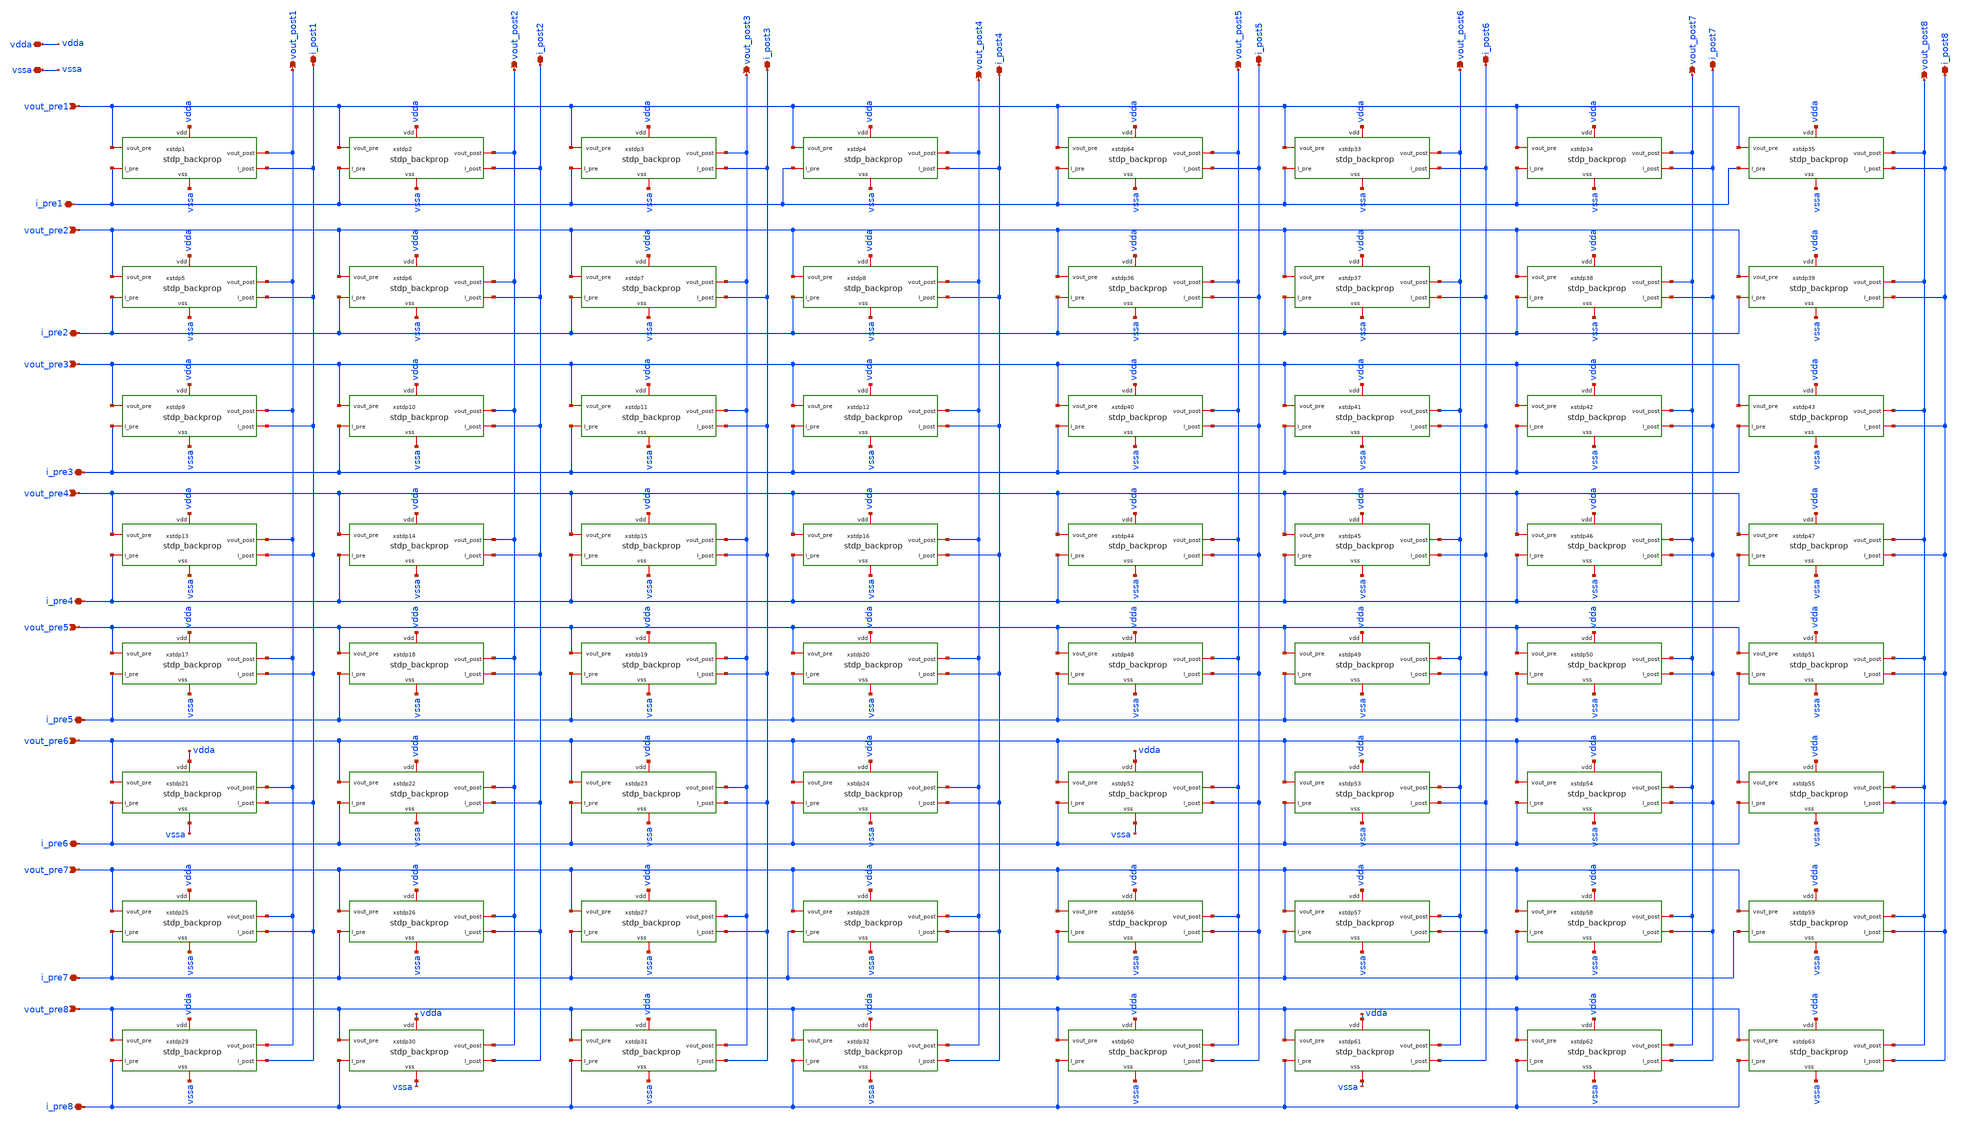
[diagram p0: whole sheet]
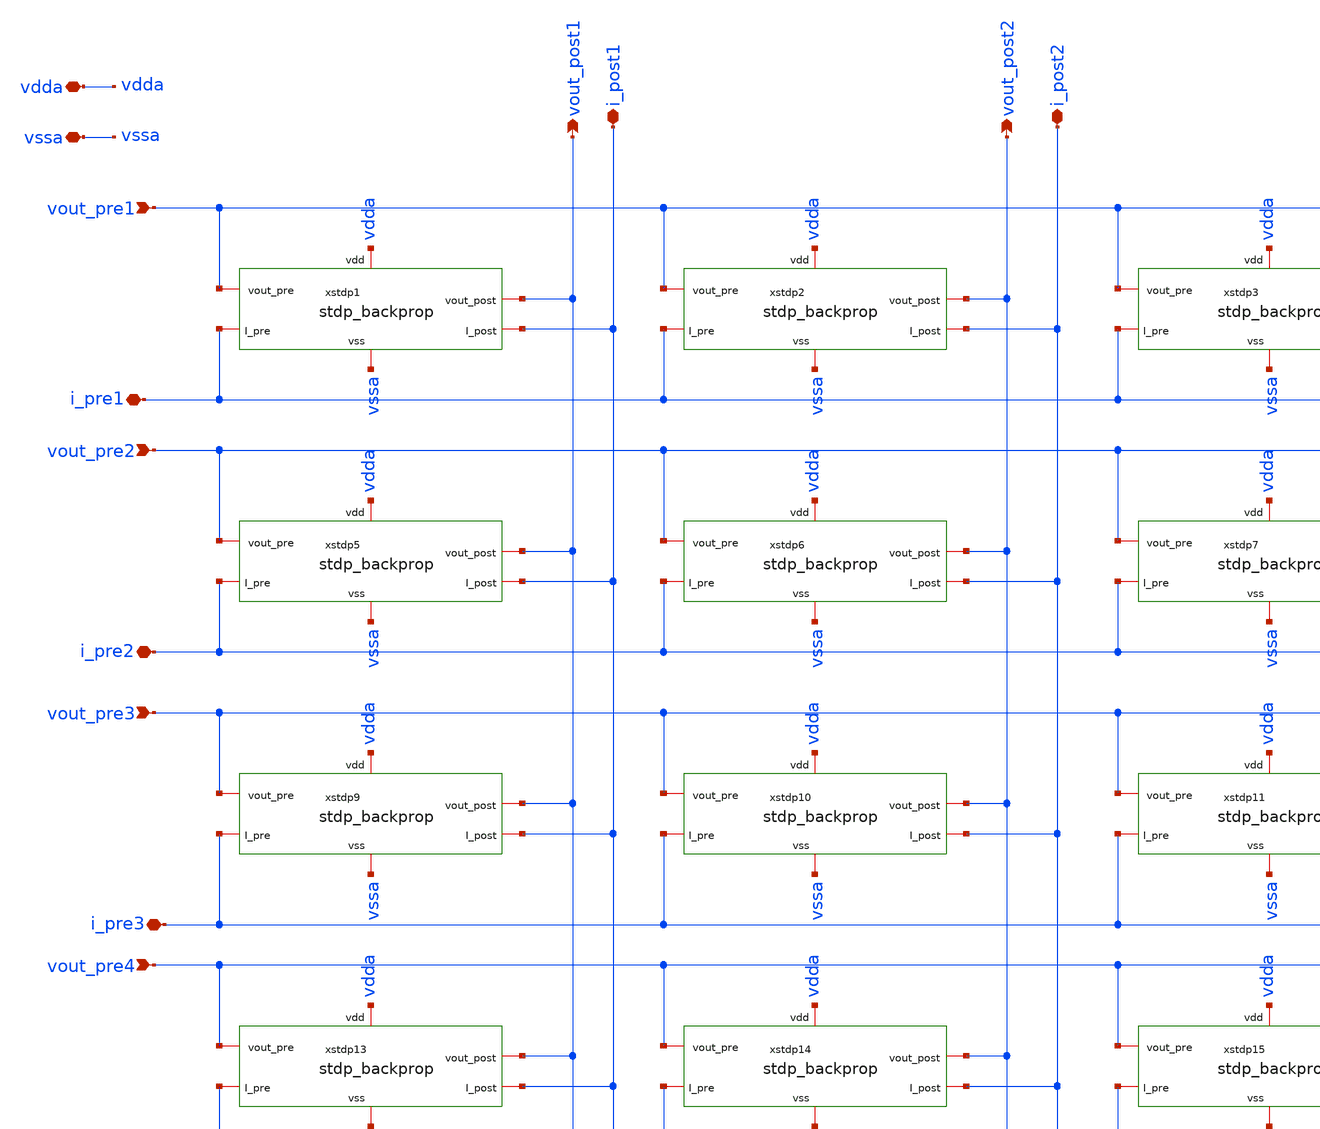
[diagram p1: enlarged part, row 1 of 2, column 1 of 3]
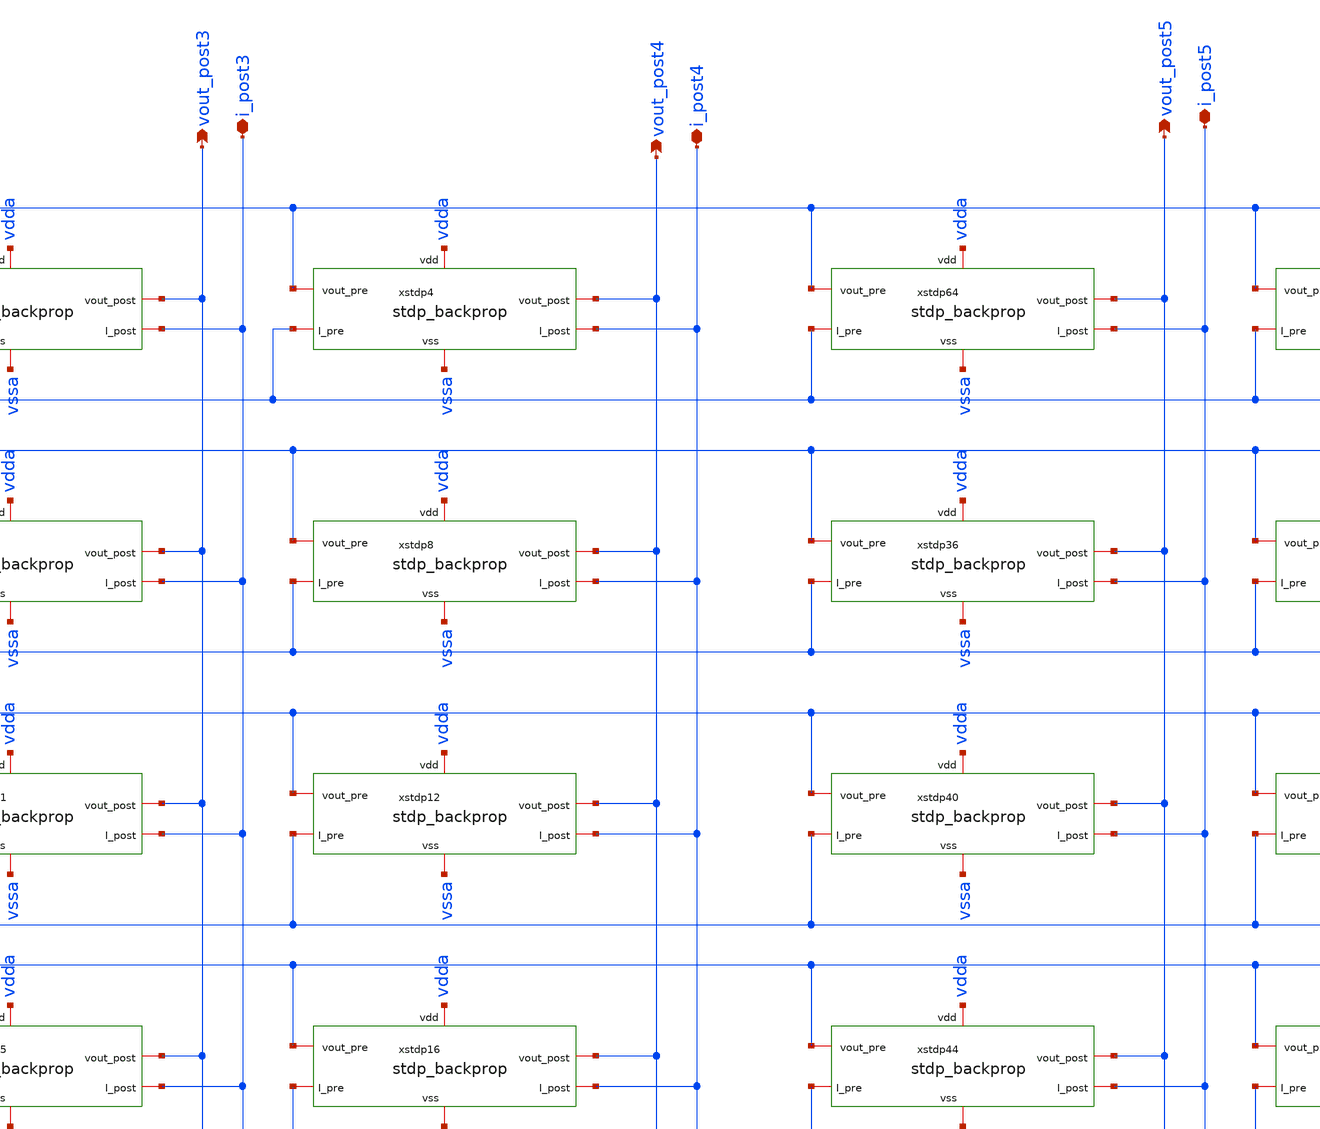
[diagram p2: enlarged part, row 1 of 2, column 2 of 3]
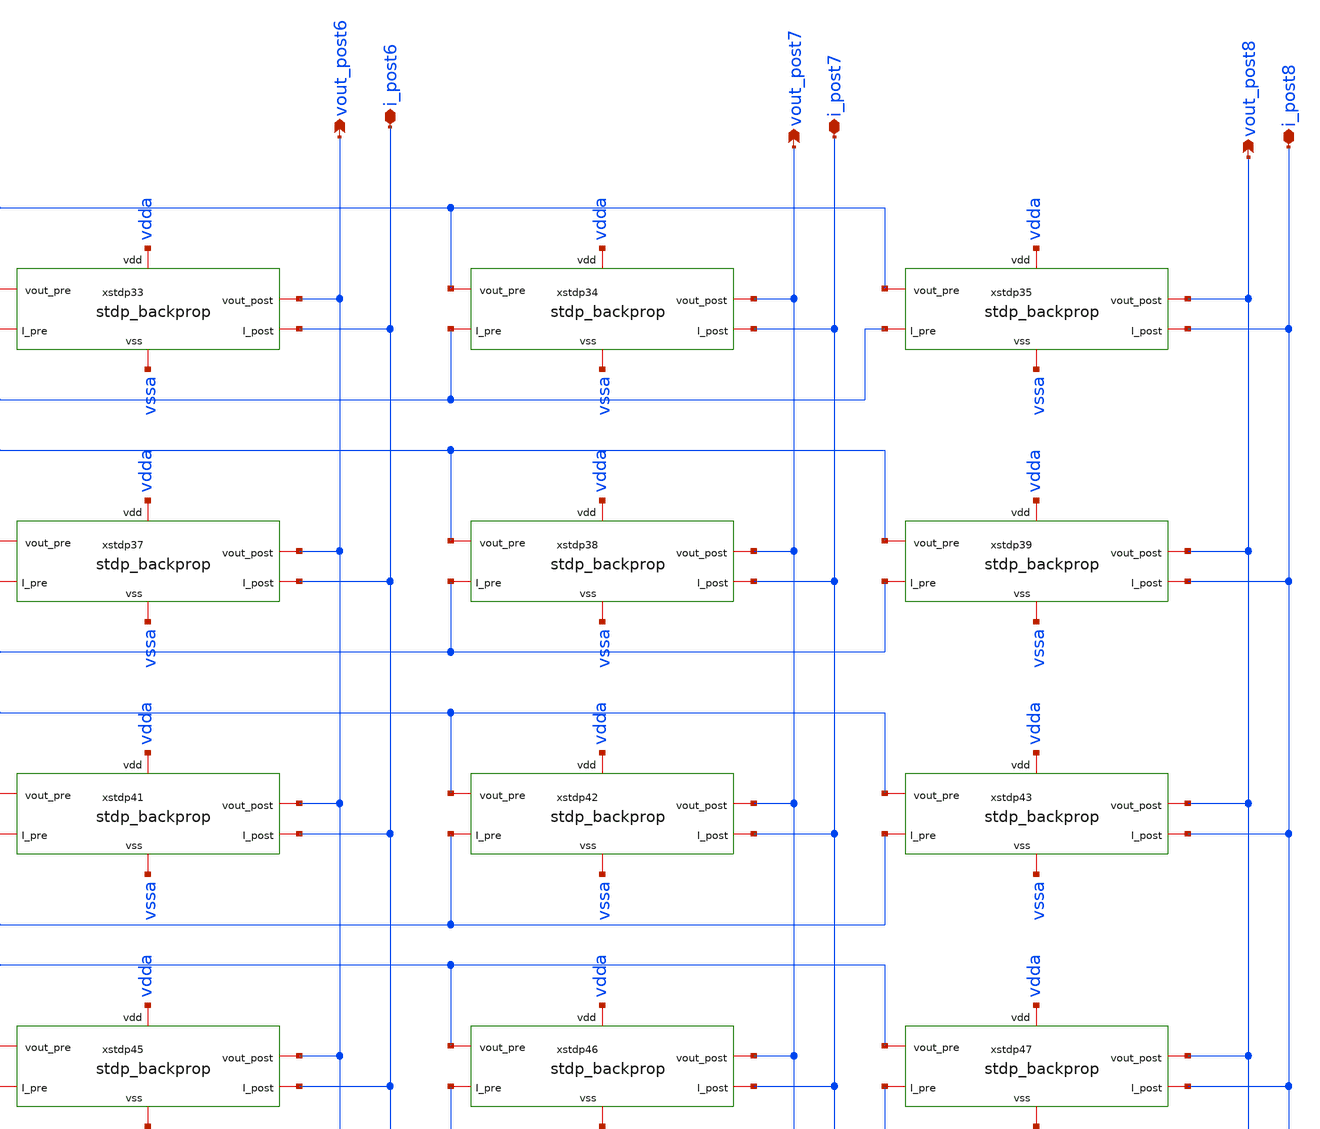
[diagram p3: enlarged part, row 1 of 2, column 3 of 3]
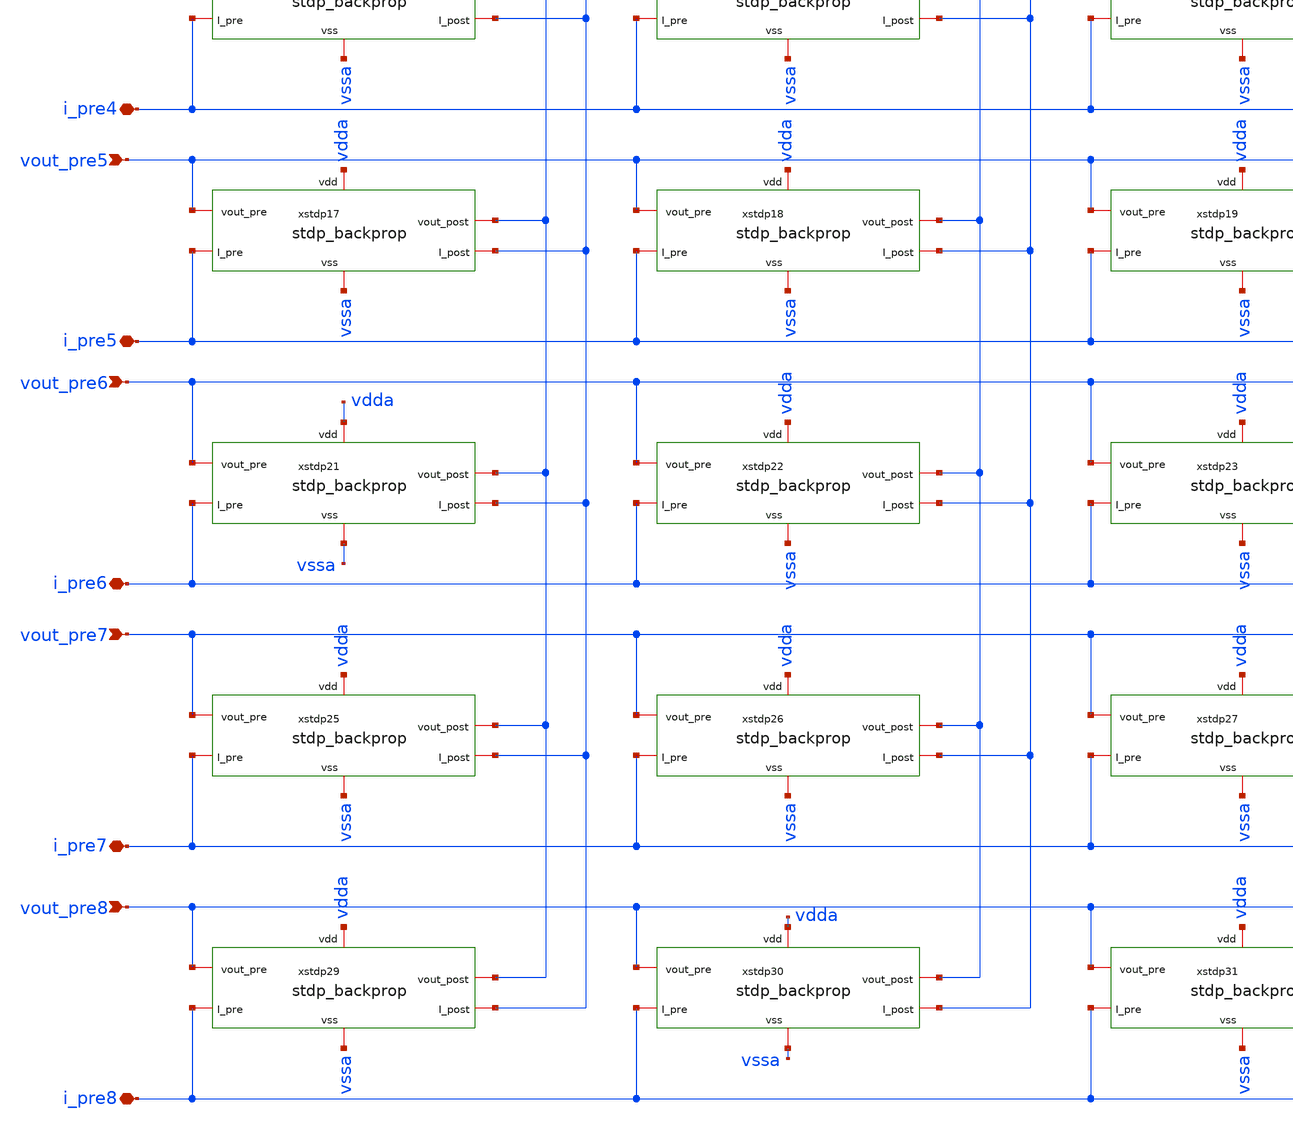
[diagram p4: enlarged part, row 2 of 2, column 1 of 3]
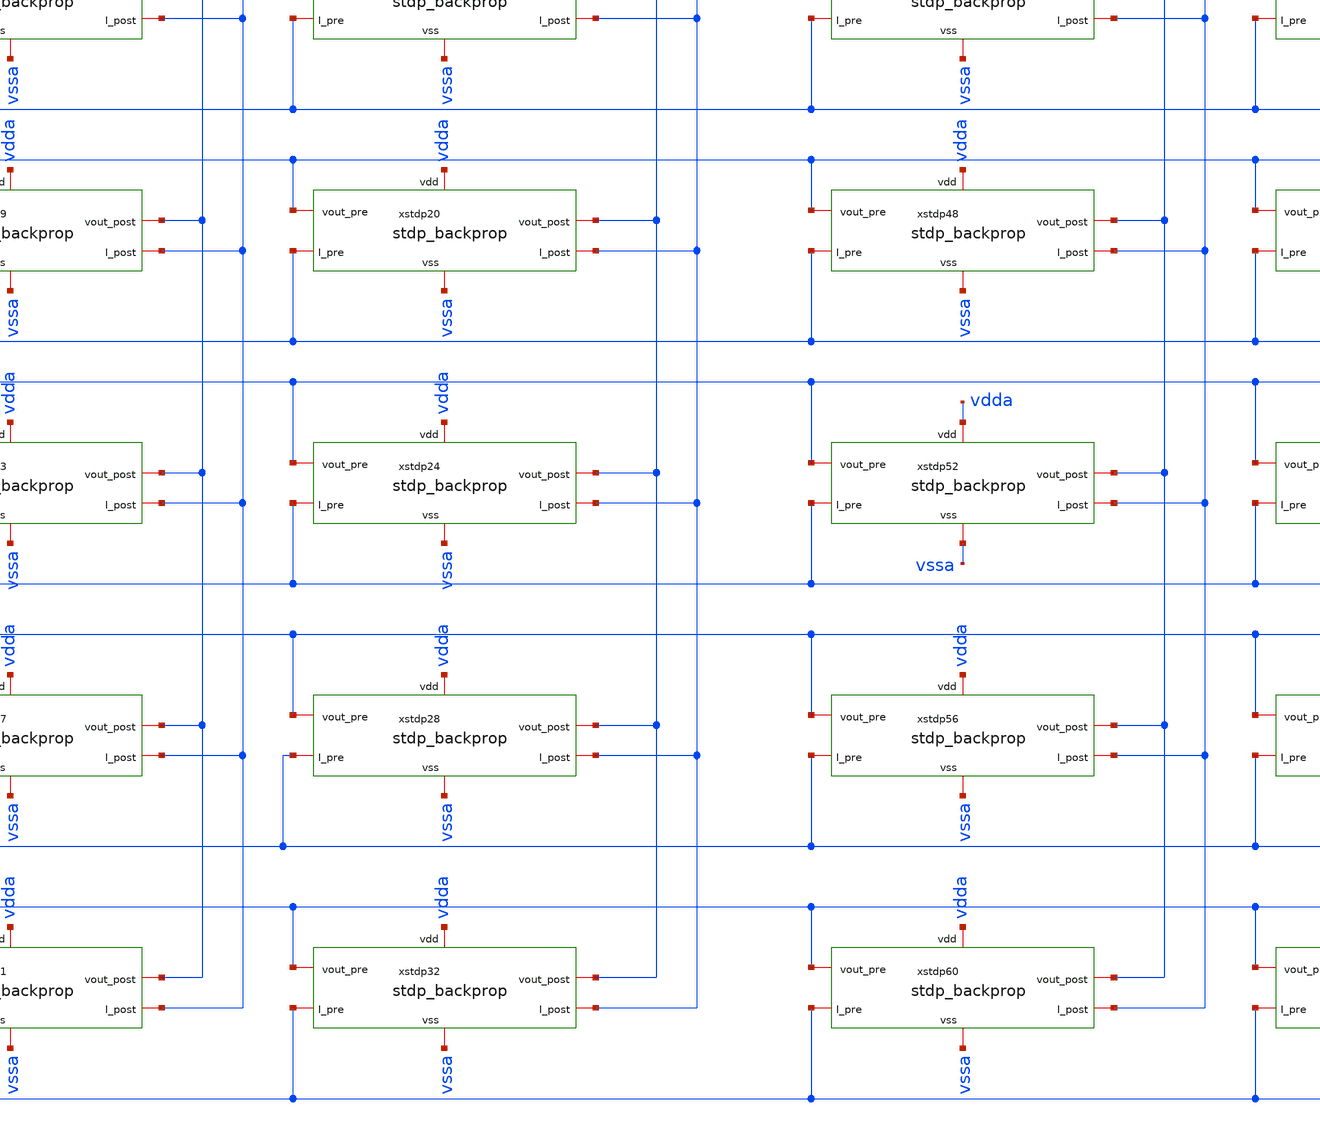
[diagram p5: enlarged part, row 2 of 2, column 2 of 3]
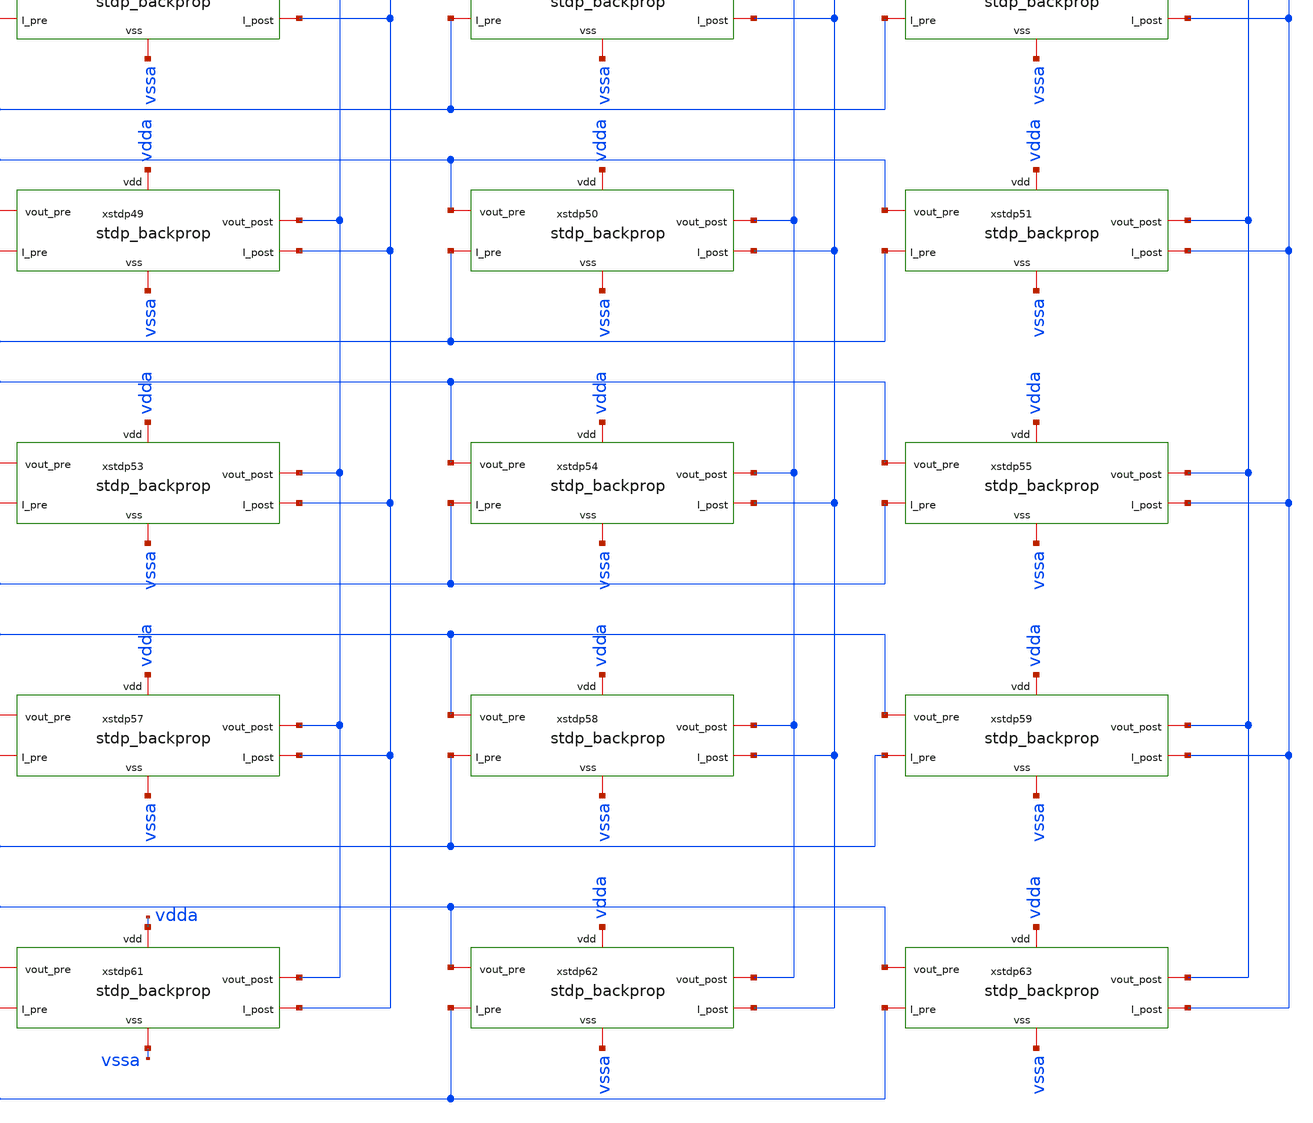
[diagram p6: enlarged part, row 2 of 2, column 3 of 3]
** sch_path: Synapse/stdp_backprop_8x8.sch
**.subckt stdp_backprop_8x8 vout_pre1 vout_post1 vdda vssa i_post1 i_post3 i_post4 vout_pre2
*+ vout_pre3 vout_pre4 vout_post2 vout_post3 vout_post4 i_post2 vout_pre5 vout_pre6 vout_pre7 vout_pre8 i_pre1
*+ i_pre2 i_pre3 i_pre4 i_pre5 i_pre6 i_pre7 i_pre8 vout_post5 i_post5 i_post7 i_post8 vout_post6 vout_post7
*+ vout_post8 i_post6
*.ipin vout_pre1
*.opin vout_post1
*.iopin vdda
*.iopin vssa
*.iopin i_post1
*.iopin i_post3
*.iopin i_post4
*.ipin vout_pre2
*.ipin vout_pre3
*.ipin vout_pre4
*.opin vout_post2
*.opin vout_post3
*.opin vout_post4
*.iopin i_post2
*.ipin vout_pre5
*.ipin vout_pre6
*.ipin vout_pre7
*.ipin vout_pre8
*.iopin i_pre1
*.iopin i_pre2
*.iopin i_pre3
*.iopin i_pre4
*.iopin i_pre5
*.iopin i_pre6
*.iopin i_pre7
*.iopin i_pre8
*.opin vout_post5
*.iopin i_post5
*.iopin i_post7
*.iopin i_post8
*.opin vout_post6
*.opin vout_post7
*.opin vout_post8
*.iopin i_post6
xstdp2 vdda vssa vout_pre1 vout_post2 i_post2 i_pre1 stdp_backprop
xstdp3 vdda vssa vout_pre1 vout_post3 i_post3 i_pre1 stdp_backprop
xstdp4 vdda vssa vout_pre1 vout_post4 i_post4 i_pre1 stdp_backprop
xstdp5 vdda vssa vout_pre2 vout_post1 i_post1 i_pre2 stdp_backprop
xstdp6 vdda vssa vout_pre2 vout_post2 i_post2 i_pre2 stdp_backprop
xstdp7 vdda vssa vout_pre2 vout_post3 i_post3 i_pre2 stdp_backprop
xstdp8 vdda vssa vout_pre2 vout_post4 i_post4 i_pre2 stdp_backprop
xstdp9 vdda vssa vout_pre3 vout_post1 i_post1 i_pre3 stdp_backprop
xstdp10 vdda vssa vout_pre3 vout_post2 i_post2 i_pre3 stdp_backprop
xstdp11 vdda vssa vout_pre3 vout_post3 i_post3 i_pre3 stdp_backprop
xstdp12 vdda vssa vout_pre3 vout_post4 i_post4 i_pre3 stdp_backprop
xstdp13 vdda vssa vout_pre4 vout_post1 i_post1 i_pre4 stdp_backprop
xstdp14 vdda vssa vout_pre4 vout_post2 i_post2 i_pre4 stdp_backprop
xstdp15 vdda vssa vout_pre4 vout_post3 i_post3 i_pre4 stdp_backprop
xstdp16 vdda vssa vout_pre4 vout_post4 i_post4 i_pre4 stdp_backprop
xstdp17 vdda vssa vout_pre5 vout_post1 i_post1 i_pre5 stdp_backprop
xstdp18 vdda vssa vout_pre5 vout_post2 i_post2 i_pre5 stdp_backprop
xstdp19 vdda vssa vout_pre5 vout_post3 i_post3 i_pre5 stdp_backprop
xstdp20 vdda vssa vout_pre5 vout_post4 i_post4 i_pre5 stdp_backprop
xstdp21 vdda vssa vout_pre6 vout_post1 i_post1 i_pre6 stdp_backprop
xstdp22 vdda vssa vout_pre6 vout_post2 i_post2 i_pre6 stdp_backprop
xstdp23 vdda vssa vout_pre6 vout_post3 i_post3 i_pre6 stdp_backprop
xstdp24 vdda vssa vout_pre6 vout_post4 i_post4 i_pre6 stdp_backprop
xstdp25 vdda vssa vout_pre7 vout_post1 i_post1 i_pre7 stdp_backprop
xstdp26 vdda vssa vout_pre7 vout_post2 i_post2 i_pre7 stdp_backprop
xstdp27 vdda vssa vout_pre7 vout_post3 i_post3 i_pre7 stdp_backprop
xstdp28 vdda vssa vout_pre7 vout_post4 i_post4 i_pre7 stdp_backprop
xstdp29 vdda vssa vout_pre8 vout_post1 i_post1 i_pre8 stdp_backprop
xstdp30 vdda vssa vout_pre8 vout_post2 i_post2 i_pre8 stdp_backprop
xstdp31 vdda vssa vout_pre8 vout_post3 i_post3 i_pre8 stdp_backprop
xstdp32 vdda vssa vout_pre8 vout_post4 i_post4 i_pre8 stdp_backprop
xstdp1 vdda vssa vout_pre1 vout_post1 i_post1 i_pre1 stdp_backprop
xstdp33 vdda vssa vout_pre1 vout_post6 i_post6 i_pre1 stdp_backprop
xstdp34 vdda vssa vout_pre1 vout_post7 i_post7 i_pre1 stdp_backprop
xstdp35 vdda vssa vout_pre1 vout_post8 i_post8 i_pre1 stdp_backprop
xstdp36 vdda vssa vout_pre2 vout_post5 i_post5 i_pre2 stdp_backprop
xstdp37 vdda vssa vout_pre2 vout_post6 i_post6 i_pre2 stdp_backprop
xstdp38 vdda vssa vout_pre2 vout_post7 i_post7 i_pre2 stdp_backprop
xstdp39 vdda vssa vout_pre2 vout_post8 i_post8 i_pre2 stdp_backprop
xstdp40 vdda vssa vout_pre3 vout_post5 i_post5 i_pre3 stdp_backprop
xstdp41 vdda vssa vout_pre3 vout_post6 i_post6 i_pre3 stdp_backprop
xstdp42 vdda vssa vout_pre3 vout_post7 i_post7 i_pre3 stdp_backprop
xstdp43 vdda vssa vout_pre3 vout_post8 i_post8 i_pre3 stdp_backprop
xstdp44 vdda vssa vout_pre4 vout_post5 i_post5 i_pre4 stdp_backprop
xstdp45 vdda vssa vout_pre4 vout_post6 i_post6 i_pre4 stdp_backprop
xstdp46 vdda vssa vout_pre4 vout_post7 i_post7 i_pre4 stdp_backprop
xstdp47 vdda vssa vout_pre4 vout_post8 i_post8 i_pre4 stdp_backprop
xstdp48 vdda vssa vout_pre5 vout_post5 i_post5 i_pre5 stdp_backprop
xstdp49 vdda vssa vout_pre5 vout_post6 i_post6 i_pre5 stdp_backprop
xstdp50 vdda vssa vout_pre5 vout_post7 i_post7 i_pre5 stdp_backprop
xstdp51 vdda vssa vout_pre5 vout_post8 i_post8 i_pre5 stdp_backprop
xstdp52 vdda vssa vout_pre6 vout_post5 i_post5 i_pre6 stdp_backprop
xstdp53 vdda vssa vout_pre6 vout_post6 i_post6 i_pre6 stdp_backprop
xstdp54 vdda vssa vout_pre6 vout_post7 i_post7 i_pre6 stdp_backprop
xstdp55 vdda vssa vout_pre6 vout_post8 i_post8 i_pre6 stdp_backprop
xstdp56 vdda vssa vout_pre7 vout_post5 i_post5 i_pre7 stdp_backprop
xstdp57 vdda vssa vout_pre7 vout_post6 i_post6 i_pre7 stdp_backprop
xstdp58 vdda vssa vout_pre7 vout_post7 i_post7 i_pre7 stdp_backprop
xstdp59 vdda vssa vout_pre7 vout_post8 i_post8 i_pre7 stdp_backprop
xstdp60 vdda vssa vout_pre8 vout_post5 i_post5 i_pre8 stdp_backprop
xstdp61 vdda vssa vout_pre8 vout_post6 i_post6 i_pre8 stdp_backprop
xstdp62 vdda vssa vout_pre8 vout_post7 i_post7 i_pre8 stdp_backprop
xstdp63 vdda vssa vout_pre8 vout_post8 i_post8 i_pre8 stdp_backprop
xstdp64 vdda vssa vout_pre1 vout_post5 i_post5 i_pre1 stdp_backprop
**.ends
.end
